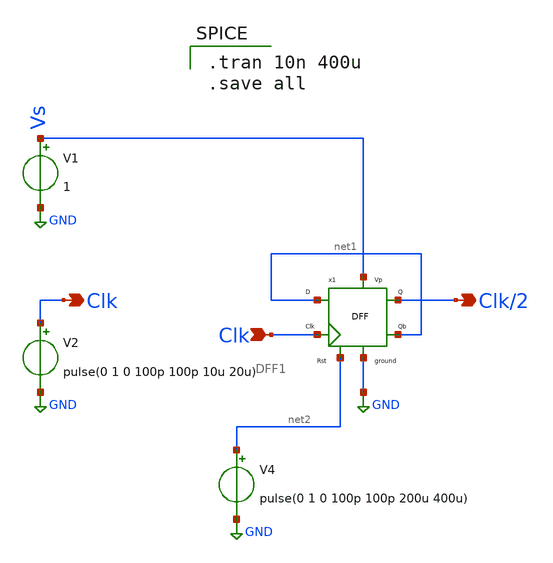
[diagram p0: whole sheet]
** sch_path: Blocks/Divide by 3 Circuit/test_b.sch
**.subckt test_b Clk Clk/2 Clk
*.opin Clk
*.opin Clk/2
*.ipin Clk
x1 net1 Clk net2 GND Vs Clk/2 net1 DFF1
V1 Vs GND 1
V2 Clk GND pulse(0 1 0 100p 100p 10u 20u)
V4 net2 GND pulse(0 1 0 100p 100p 200u 400u)
**** begin user architecture code

** opencircuitdesign pdks install
.lib $::SKYWATER_MODELS/sky130.lib.spice tt



.tran 10n 400u
.save all

**** end user architecture code
**.ends

* expanding   symbol:  Pico_project/FlipFlops/DFF1.sym # of pins=7
** sym_path: component/FlipFlops/DFF1.sym
** sch_path: component/FlipFlops/DFF1.sch
.subckt DFF1 D Clk RST VN VP Q Qb
*.opin Q
*.iopin VN
*.iopin VP
*.ipin Clk
*.ipin D
*.ipin RST
*.opin Qb
x7 net2 net4 net3 VP VN NAND
x8 net3 Clk RST VP VN net2 NAND3
x6 Q net1 RST VP VN Qb NAND3
x4 net2 Clk net4 VP VN net1 NAND3
x5 net1 D RST VP VN net4 NAND3
x1 Qb net2 Q VP VN NAND
.ends


* expanding   symbol:  component/NAND2/NAND.sym # of pins=5
** sym_path: component/NAND2/NAND.sym
** sch_path: component/NAND2/NAND.sch
.subckt NAND B A Y VP VN
*.iopin VP
*.ipin A
*.ipin B
*.opin Y
*.iopin VN
XM1 Y A VP VP sky130_fd_pr__pfet_01v8 L=0.15 W=1.26 nf=1 ad='int((nf+1)/2) * W/nf * 0.29' as='int((nf+2)/2) * W/nf * 0.29'
+ pd='2*int((nf+1)/2) * (W/nf + 0.29)' ps='2*int((nf+2)/2) * (W/nf + 0.29)' nrd='0.29 / W' nrs='0.29 / W'
+ sa=0 sb=0 sd=0 mult=1 m=1
XM2 Y B VP VP sky130_fd_pr__pfet_01v8 L=0.15 W=1.26 nf=1 ad='int((nf+1)/2) * W/nf * 0.29' as='int((nf+2)/2) * W/nf * 0.29'
+ pd='2*int((nf+1)/2) * (W/nf + 0.29)' ps='2*int((nf+2)/2) * (W/nf + 0.29)' nrd='0.29 / W' nrs='0.29 / W'
+ sa=0 sb=0 sd=0 mult=1 m=1
XM3 Y A net1 net1 sky130_fd_pr__nfet_01v8 L=0.15 W=0.84 nf=1 ad='int((nf+1)/2) * W/nf * 0.29' as='int((nf+2)/2) * W/nf * 0.29'
+ pd='2*int((nf+1)/2) * (W/nf + 0.29)' ps='2*int((nf+2)/2) * (W/nf + 0.29)' nrd='0.29 / W' nrs='0.29 / W'
+ sa=0 sb=0 sd=0 mult=1 m=1
XM4 net1 B VN VN sky130_fd_pr__nfet_01v8 L=0.15 W=0.84 nf=1 ad='int((nf+1)/2) * W/nf * 0.29' as='int((nf+2)/2) * W/nf * 0.29'
+ pd='2*int((nf+1)/2) * (W/nf + 0.29)' ps='2*int((nf+2)/2) * (W/nf + 0.29)' nrd='0.29 / W' nrs='0.29 / W'
+ sa=0 sb=0 sd=0 mult=1 m=1
.ends


* expanding   symbol:  component/NAND3/NAND3.sym # of pins=6
** sym_path: component/NAND3/NAND3.sym
** sch_path: component/NAND3/NAND3.sch
.subckt NAND3 A B C VP VN Y
*.iopin VP
*.iopin VN
*.ipin A
*.ipin B
*.ipin C
*.opin Y
XM1 Y A net1 VN sky130_fd_pr__nfet_01v8 L=0.15 W=1.26 nf=1 ad='int((nf+1)/2) * W/nf * 0.29' as='int((nf+2)/2) * W/nf * 0.29'
+ pd='2*int((nf+1)/2) * (W/nf + 0.29)' ps='2*int((nf+2)/2) * (W/nf + 0.29)' nrd='0.29 / W' nrs='0.29 / W'
+ sa=0 sb=0 sd=0 mult=1 m=1
XM2 net1 B net2 VN sky130_fd_pr__nfet_01v8 L=0.15 W=1.26 nf=1 ad='int((nf+1)/2) * W/nf * 0.29' as='int((nf+2)/2) * W/nf * 0.29'
+ pd='2*int((nf+1)/2) * (W/nf + 0.29)' ps='2*int((nf+2)/2) * (W/nf + 0.29)' nrd='0.29 / W' nrs='0.29 / W'
+ sa=0 sb=0 sd=0 mult=1 m=1
XM3 net2 C VN VN sky130_fd_pr__nfet_01v8 L=0.15 W=1.26 nf=1 ad='int((nf+1)/2) * W/nf * 0.29' as='int((nf+2)/2) * W/nf * 0.29'
+ pd='2*int((nf+1)/2) * (W/nf + 0.29)' ps='2*int((nf+2)/2) * (W/nf + 0.29)' nrd='0.29 / W' nrs='0.29 / W'
+ sa=0 sb=0 sd=0 mult=1 m=1
XM4 Y A VP VP sky130_fd_pr__pfet_01v8 L=0.15 W=1.26 nf=1 ad='int((nf+1)/2) * W/nf * 0.29' as='int((nf+2)/2) * W/nf * 0.29'
+ pd='2*int((nf+1)/2) * (W/nf + 0.29)' ps='2*int((nf+2)/2) * (W/nf + 0.29)' nrd='0.29 / W' nrs='0.29 / W'
+ sa=0 sb=0 sd=0 mult=1 m=1
XM5 Y B VP VP sky130_fd_pr__pfet_01v8 L=0.15 W=1.26 nf=1 ad='int((nf+1)/2) * W/nf * 0.29' as='int((nf+2)/2) * W/nf * 0.29'
+ pd='2*int((nf+1)/2) * (W/nf + 0.29)' ps='2*int((nf+2)/2) * (W/nf + 0.29)' nrd='0.29 / W' nrs='0.29 / W'
+ sa=0 sb=0 sd=0 mult=1 m=1
XM6 Y C VP VP sky130_fd_pr__pfet_01v8 L=0.15 W=1.26 nf=1 ad='int((nf+1)/2) * W/nf * 0.29' as='int((nf+2)/2) * W/nf * 0.29'
+ pd='2*int((nf+1)/2) * (W/nf + 0.29)' ps='2*int((nf+2)/2) * (W/nf + 0.29)' nrd='0.29 / W' nrs='0.29 / W'
+ sa=0 sb=0 sd=0 mult=1 m=1
.ends

.GLOBAL GND
.end
